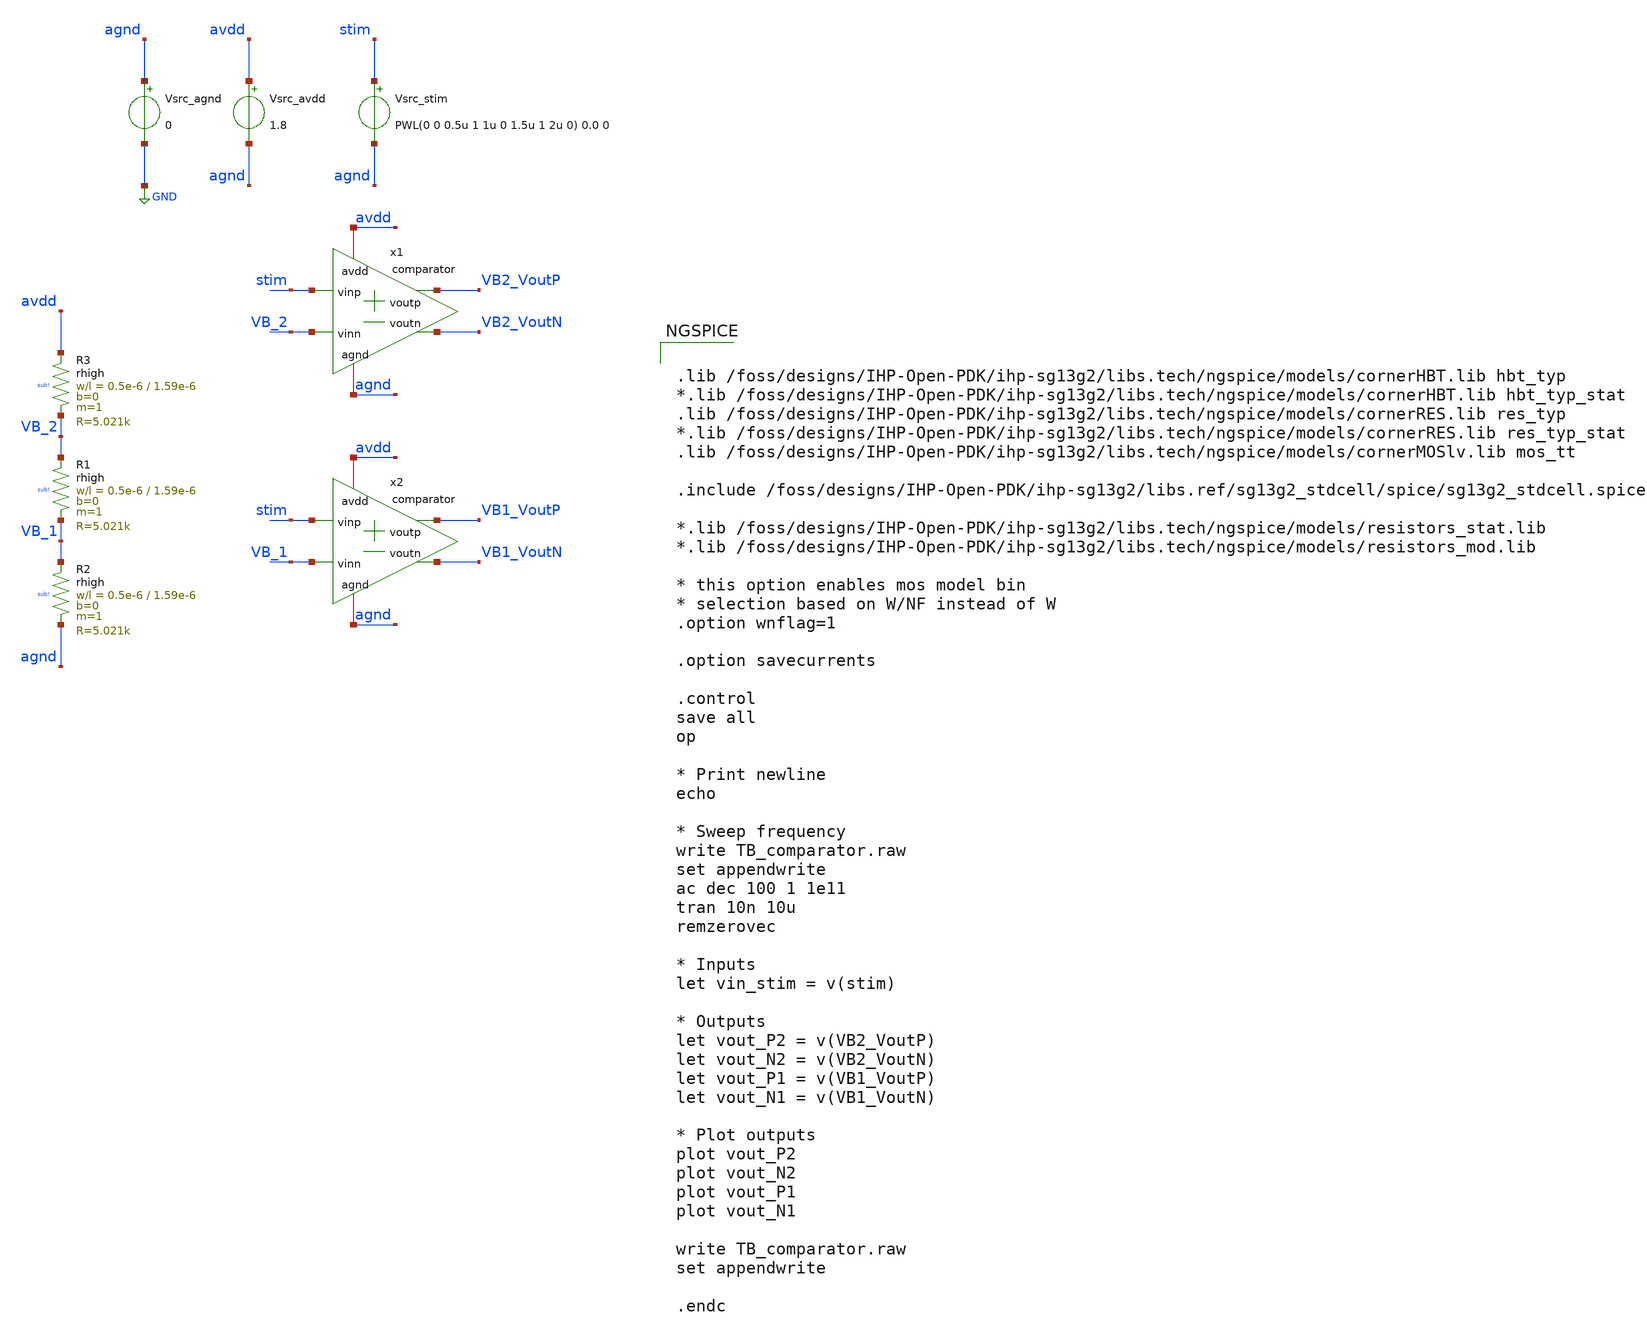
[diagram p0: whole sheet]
** sch_path: xschem/TB_comparator.sch
**.subckt TB_comparator
x1 avdd VB2_VoutP VB2_VoutN VB_2 stim agnd comparator
Vsrc_agnd agnd GND 0
Vsrc_avdd avdd agnd 1.8
x2 avdd VB1_VoutP VB1_VoutN VB_1 stim agnd comparator
XR3 avdd VB_2 sub! rhigh w=0.5e-6 l=1.59e-6 m=1 b=0 mm_ok=1
XR1 VB_2 VB_1 sub! rhigh w=0.5e-6 l=1.59e-6 m=1 b=0 mm_ok=1
XR2 VB_1 agnd sub! rhigh w=0.5e-6 l=1.59e-6 m=1 b=0 mm_ok=1
Vsrc_stim stim agnd PWL(0 0 0.5u 1 1u 0 1.5u 1 2u 0) 0.0 0
**** begin user architecture code


.lib /foss/designs/IHP-Open-PDK/ihp-sg13g2/libs.tech/ngspice/models/cornerHBT.lib hbt_typ
*.lib /foss/designs/IHP-Open-PDK/ihp-sg13g2/libs.tech/ngspice/models/cornerHBT.lib hbt_typ_stat
.lib /foss/designs/IHP-Open-PDK/ihp-sg13g2/libs.tech/ngspice/models/cornerRES.lib res_typ
*.lib /foss/designs/IHP-Open-PDK/ihp-sg13g2/libs.tech/ngspice/models/cornerRES.lib res_typ_stat
.lib /foss/designs/IHP-Open-PDK/ihp-sg13g2/libs.tech/ngspice/models/cornerMOSlv.lib mos_tt

.include /foss/designs/IHP-Open-PDK/ihp-sg13g2/libs.ref/sg13g2_stdcell/spice/sg13g2_stdcell.spice

*.lib /foss/designs/IHP-Open-PDK/ihp-sg13g2/libs.tech/ngspice/models/resistors_stat.lib
*.lib /foss/designs/IHP-Open-PDK/ihp-sg13g2/libs.tech/ngspice/models/resistors_mod.lib

* this option enables mos model bin
* selection based on W/NF instead of W
.option wnflag=1

.option savecurrents

.control
save all
op

* Print newline
echo

* Sweep frequency
write TB_comparator.raw
set appendwrite
ac dec 100 1 1e11
tran 10n 10u
remzerovec

* Inputs
let vin_stim = v(stim)

* Outputs
let vout_P2 = v(VB2_VoutP)
let vout_N2 = v(VB2_VoutN)
let vout_P1 = v(VB1_VoutP)
let vout_N1 = v(VB1_VoutN)

* Plot outputs
plot vout_P2
plot vout_N2
plot vout_P1
plot vout_N1

write TB_comparator.raw
set appendwrite

.endc


**** end user architecture code
**.ends

* expanding   symbol:  /foss/designs/Tiny_Tapeout/TTIHP0p3_HBT_555_Timer/xschem/comparator.sym # of
*+ pins=6
** sym_path: xschem/comparator.sym
** sch_path: xschem/comparator.sch
.subckt comparator avdd voutp voutn vinn vinp agnd
*.iopin avdd
*.ipin vinp
*.opin voutp
*.iopin agnd
*.ipin vinn
*.opin voutn
XR2 net1 agnd sub! rppd w=0.5e-6 l=7.5e-6 m=1 b=0 mm_ok=1
XQ1 voutp vinn net1 agnd npn13G2 Nx=1 mm_ok=1
XQ2 voutn vinp net1 agnd npn13G2 Nx=1 mm_ok=1
XR1 avdd voutp sub! rppd w=0.5e-6 l=7.5e-6 m=1 b=0 mm_ok=1
XR3 avdd voutn sub! rppd w=0.5e-6 l=7.5e-6 m=1 b=0 mm_ok=1
.ends

.GLOBAL GND
.end
